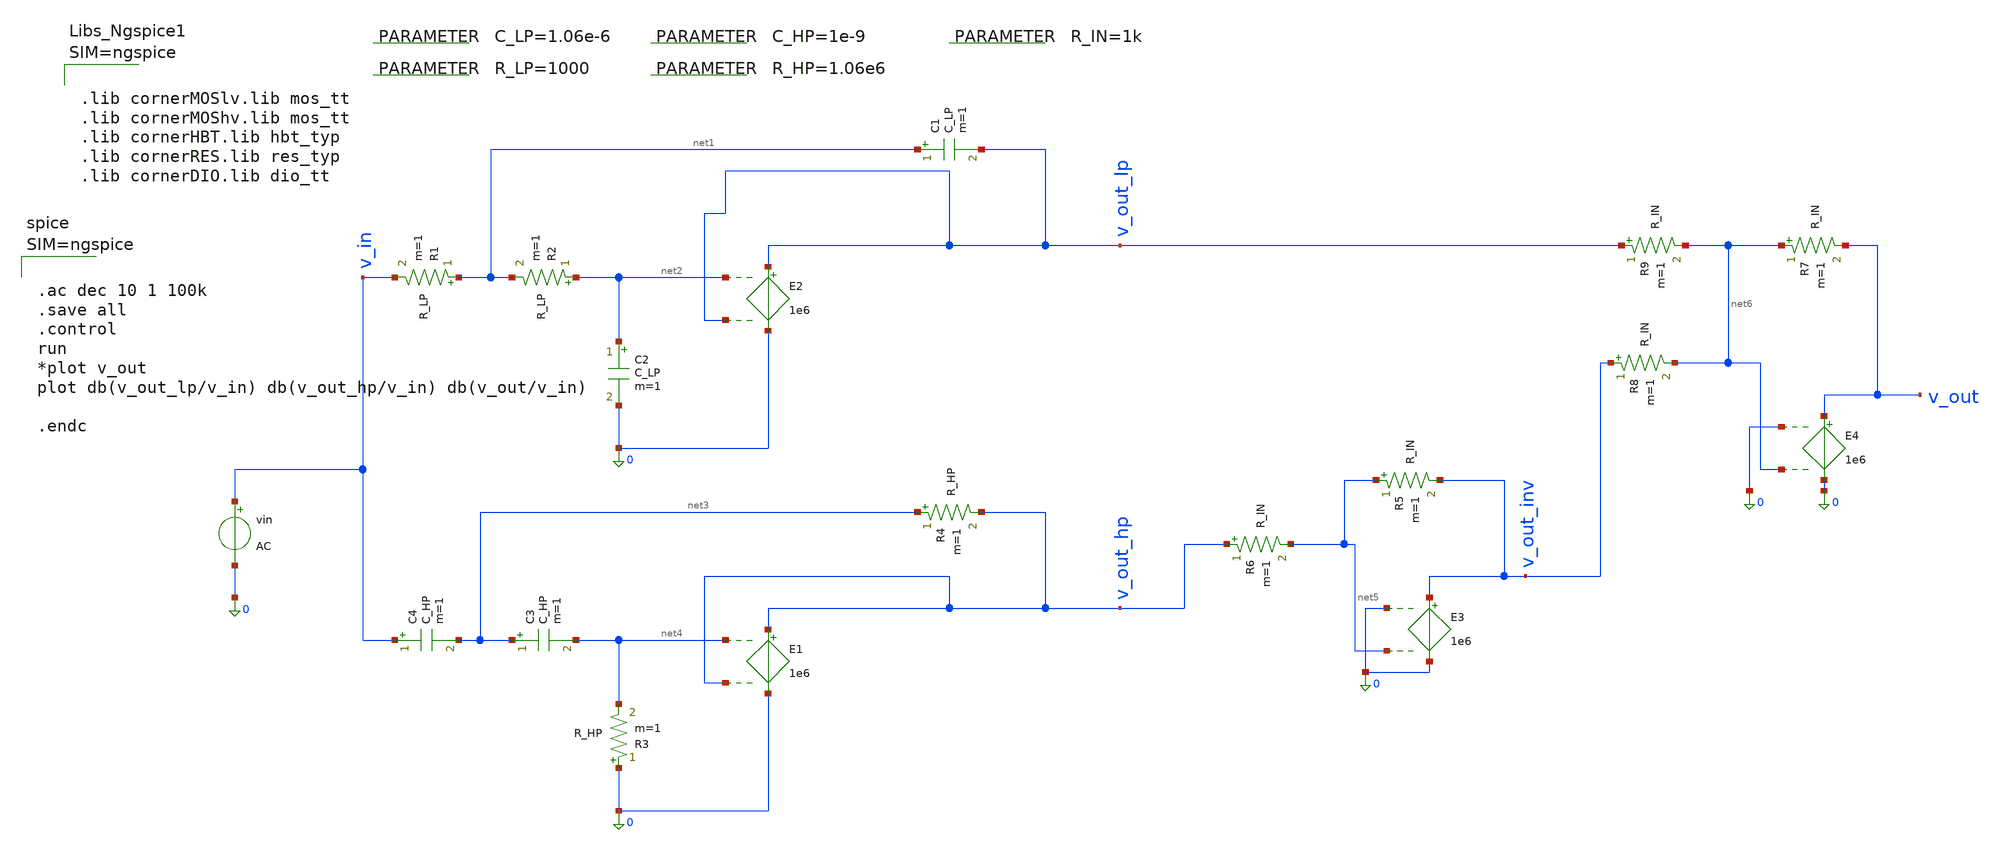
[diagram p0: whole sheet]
** sch_path: 003_Ideal_Circuits/linkwitz_riley_cross_vsvc_150hz.sch
**.subckt linkwitz_riley_cross_vsvc_150hz
R1 net1 v_in R_LP m=1
R2 net2 net1 R_LP m=1
C1 net1 v_out_lp C_LP m=1
C2 net2 0 C_LP m=1
vin v_in 0 AC
.param C_LP=1.06e-6
.param R_LP=1000
R3 0 net4 R_HP m=1
R4 net3 v_out_hp R_HP m=1
C3 net3 net4 C_HP m=1
C4 v_in net3 C_HP m=1
.param C_HP=1e-9
.param R_HP=1.06e6
R5 net5 v_out_inv R_IN m=1
R6 v_out_hp net5 R_IN m=1
.param R_IN=1k
R7 net6 v_out R_IN m=1
R8 v_out_inv net6 R_IN m=1
R9 v_out_lp net6 R_IN m=1
E2 v_out_lp 0 net2 v_out_lp 1e6
E1 v_out_hp 0 net4 v_out_hp 1e6
E3 v_out_inv 0 0 net5 1e6
E4 v_out 0 0 net6 1e6
**** begin user architecture code



.lib cornerMOSlv.lib mos_tt
.lib cornerMOShv.lib mos_tt
.lib cornerHBT.lib hbt_typ
.lib cornerRES.lib res_typ
.lib cornerDIO.lib dio_tt






.ac dec 10 1 100k
.save all
.control
run
*plot v_out
plot db(v_out_lp/v_in) db(v_out_hp/v_in) db(v_out/v_in)

.endc



**** end user architecture code
**.ends
.end
